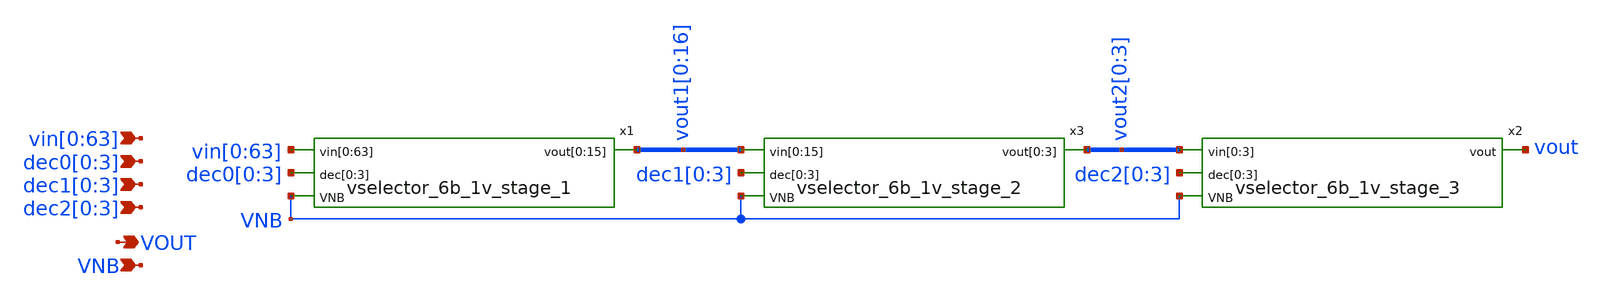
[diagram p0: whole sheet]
** sch_path: xschem/vselector_6b_1v.sch
**.subckt vselector_6b_1v
*+ vin[0],vin[1],vin[2],vin[3],vin[4],vin[5],vin[6],vin[7],vin[8],vin[9],vin[10],vin[11],vin[12],vin[13],vin[14],vin[15],vin[16],vin[17],vin[18],vin[19],vin[20],vin[21],vin[22],vin[23],vin[24],vin[25],vin[26],vin[27],vin[28],vin[29],vin[30],vin[31],vin[32],vin[33],vin[34],vin[35],vin[36],vin[37],vin[38],vin[39],vin[40],vin[41],vin[42],vin[43],vin[44],vin[45],vin[46],vin[47],vin[48],vin[49],vin[50],vin[51],vin[52],vin[53],vin[54],vin[55],vin[56],vin[57],vin[58],vin[59],vin[60],vin[61],vin[62],vin[63] VOUT VNB dec0[0],dec0[1],dec0[2],dec0[3] dec1[0],dec1[1],dec1[2],dec1[3]
*+ dec2[0],dec2[1],dec2[2],dec2[3]
*.ipin
*+ vin[0],vin[1],vin[2],vin[3],vin[4],vin[5],vin[6],vin[7],vin[8],vin[9],vin[10],vin[11],vin[12],vin[13],vin[14],vin[15],vin[16],vin[17],vin[18],vin[19],vin[20],vin[21],vin[22],vin[23],vin[24],vin[25],vin[26],vin[27],vin[28],vin[29],vin[30],vin[31],vin[32],vin[33],vin[34],vin[35],vin[36],vin[37],vin[38],vin[39],vin[40],vin[41],vin[42],vin[43],vin[44],vin[45],vin[46],vin[47],vin[48],vin[49],vin[50],vin[51],vin[52],vin[53],vin[54],vin[55],vin[56],vin[57],vin[58],vin[59],vin[60],vin[61],vin[62],vin[63]
*.opin VOUT
*.ipin VNB
*.ipin dec0[0],dec0[1],dec0[2],dec0[3]
*.ipin dec1[0],dec1[1],dec1[2],dec1[3]
*.ipin dec2[0],dec2[1],dec2[2],dec2[3]
x2 vout2[0] vout2[1] vout2[2] vout2[3] dec2[0] dec2[1] dec2[2] dec2[3] vout VNB
+ vselector_6b_1v_stage_3
x1 vin[0] vin[1] vin[2] vin[3] vin[4] vin[5] vin[6] vin[7] vin[8] vin[9] vin[10] vin[11] vin[12]
+ vin[13] vin[14] vin[15] vin[16] vin[17] vin[18] vin[19] vin[20] vin[21] vin[22] vin[23] vin[24] vin[25]
+ vin[26] vin[27] vin[28] vin[29] vin[30] vin[31] vin[32] vin[33] vin[34] vin[35] vin[36] vin[37] vin[38]
+ vin[39] vin[40] vin[41] vin[42] vin[43] vin[44] vin[45] vin[46] vin[47] vin[48] vin[49] vin[50] vin[51]
+ vin[52] vin[53] vin[54] vin[55] vin[56] vin[57] vin[58] vin[59] vin[60] vin[61] vin[62] vin[63] dec0[0]
+ dec0[1] dec0[2] dec0[3] vout1[0] vout1[1] vout1[2] vout1[3] vout1[4] vout1[5] vout1[6] vout1[7] vout1[8]
+ vout1[9] vout1[10] vout1[11] vout1[12] vout1[13] vout1[14] vout1[15] VNB vselector_6b_1v_stage_1
x3 vout1[0] vout1[1] vout1[2] vout1[3] vout1[4] vout1[5] vout1[6] vout1[7] vout1[8] vout1[9]
+ vout1[10] vout1[11] vout1[12] vout1[13] vout1[14] vout1[15] dec1[0] dec1[1] dec1[2] dec1[3] vout2[0] vout2[1]
+ vout2[2] vout2[3] VNB vselector_6b_1v_stage_2
**.ends

* expanding   symbol:  vselector_6b_1v_stage_3.sym # of pins=4
** sym_path: xschem/vselector_6b_1v_stage_3.sym
** sch_path: xschem/vselector_6b_1v_stage_3.sch
.subckt vselector_6b_1v_stage_3 vin[0] vin[1] vin[2] vin[3] dec[0] dec[1] dec[2] dec[3] vout VNB
*.ipin vin[0],vin[1],vin[2],vin[3]
*.opin vout
*.ipin VNB
*.ipin dec[0],dec[1],dec[2],dec[3]
.param wp=0.42 wn=0.42 l=0.5

XM1 vout dec[0] vin[0] VNB sky130_fd_pr__nfet_g5v0d10v5 L=l W=wn nf=1 ad='int((nf+1)/2) * W/nf * 0.29'
+ as='int((nf+2)/2) * W/nf * 0.29' pd='2*int((nf+1)/2) * (W/nf + 0.29)' ps='2*int((nf+2)/2) * (W/nf + 0.29)'
+ nrd='0.29 / W' nrs='0.29 / W' sa=0 sb=0 sd=0 mult=1 m=1
XM2 vout dec[1] vin[1] VNB sky130_fd_pr__nfet_g5v0d10v5 L=l W=wn nf=1 ad='int((nf+1)/2) * W/nf * 0.29'
+ as='int((nf+2)/2) * W/nf * 0.29' pd='2*int((nf+1)/2) * (W/nf + 0.29)' ps='2*int((nf+2)/2) * (W/nf + 0.29)'
+ nrd='0.29 / W' nrs='0.29 / W' sa=0 sb=0 sd=0 mult=1 m=1
XM3 vout dec[2] vin[2] VNB sky130_fd_pr__nfet_g5v0d10v5 L=l W=wn nf=1 ad='int((nf+1)/2) * W/nf * 0.29'
+ as='int((nf+2)/2) * W/nf * 0.29' pd='2*int((nf+1)/2) * (W/nf + 0.29)' ps='2*int((nf+2)/2) * (W/nf + 0.29)'
+ nrd='0.29 / W' nrs='0.29 / W' sa=0 sb=0 sd=0 mult=1 m=1
XM4 vout dec[3] vin[3] VNB sky130_fd_pr__nfet_g5v0d10v5 L=l W=wn nf=1 ad='int((nf+1)/2) * W/nf * 0.29'
+ as='int((nf+2)/2) * W/nf * 0.29' pd='2*int((nf+1)/2) * (W/nf + 0.29)' ps='2*int((nf+2)/2) * (W/nf + 0.29)'
+ nrd='0.29 / W' nrs='0.29 / W' sa=0 sb=0 sd=0 mult=1 m=1
.ends


* expanding   symbol:  vselector_6b_1v_stage_1.sym # of pins=4
** sym_path: xschem/vselector_6b_1v_stage_1.sym
** sch_path: xschem/vselector_6b_1v_stage_1.sch
.subckt vselector_6b_1v_stage_1 vin[0] vin[1] vin[2] vin[3] vin[4] vin[5] vin[6] vin[7] vin[8]
+ vin[9] vin[10] vin[11] vin[12] vin[13] vin[14] vin[15] vin[16] vin[17] vin[18] vin[19] vin[20] vin[21]
+ vin[22] vin[23] vin[24] vin[25] vin[26] vin[27] vin[28] vin[29] vin[30] vin[31] vin[32] vin[33] vin[34]
+ vin[35] vin[36] vin[37] vin[38] vin[39] vin[40] vin[41] vin[42] vin[43] vin[44] vin[45] vin[46] vin[47]
+ vin[48] vin[49] vin[50] vin[51] vin[52] vin[53] vin[54] vin[55] vin[56] vin[57] vin[58] vin[59] vin[60]
+ vin[61] vin[62] vin[63] dec[0] dec[1] dec[2] dec[3] vout[0] vout[1] vout[2] vout[3] vout[4] vout[5] vout[6]
+ vout[7] vout[8] vout[9] vout[10] vout[11] vout[12] vout[13] vout[14] vout[15] VNB
*.ipin
*+ vin[0],vin[1],vin[2],vin[3],vin[4],vin[5],vin[6],vin[7],vin[8],vin[9],vin[10],vin[11],vin[12],vin[13],vin[14],vin[15],vin[16],vin[17],vin[18],vin[19],vin[20],vin[21],vin[22],vin[23],vin[24],vin[25],vin[26],vin[27],vin[28],vin[29],vin[30],vin[31],vin[32],vin[33],vin[34],vin[35],vin[36],vin[37],vin[38],vin[39],vin[40],vin[41],vin[42],vin[43],vin[44],vin[45],vin[46],vin[47],vin[48],vin[49],vin[50],vin[51],vin[52],vin[53],vin[54],vin[55],vin[56],vin[57],vin[58],vin[59],vin[60],vin[61],vin[62],vin[63]
*.opin
*+ vout[0],vout[1],vout[2],vout[3],vout[4],vout[5],vout[6],vout[7],vout[8],vout[9],vout[10],vout[11],vout[12],vout[13],vout[14],vout[15]
*.ipin VNB
*.ipin dec[0],dec[1],dec[2],dec[3]
x1 vin[48] vin[49] vin[50] vin[51] vin[52] vin[53] vin[54] vin[55] vin[56] vin[57] vin[58] vin[59]
+ vin[60] vin[61] vin[62] vin[63] dec[3] vout[0] vout[1] vout[2] vout[3] vout[4] vout[5] vout[6] vout[7]
+ vout[8] vout[9] vout[10] vout[11] vout[12] vout[13] vout[14] vout[15] VNB vselector_16b_1v
x2 vin[32] vin[33] vin[34] vin[35] vin[36] vin[37] vin[38] vin[39] vin[40] vin[41] vin[42] vin[43]
+ vin[44] vin[45] vin[46] vin[47] dec[2] vout[0] vout[1] vout[2] vout[3] vout[4] vout[5] vout[6] vout[7]
+ vout[8] vout[9] vout[10] vout[11] vout[12] vout[13] vout[14] vout[15] VNB vselector_16b_1v
x3 vin[16] vin[17] vin[18] vin[19] vin[20] vin[21] vin[22] vin[23] vin[24] vin[25] vin[26] vin[27]
+ vin[28] vin[29] vin[30] vin[31] dec[1] vout[0] vout[1] vout[2] vout[3] vout[4] vout[5] vout[6] vout[7]
+ vout[8] vout[9] vout[10] vout[11] vout[12] vout[13] vout[14] vout[15] VNB vselector_16b_1v
x4 vin[0] vin[1] vin[2] vin[3] vin[4] vin[5] vin[6] vin[7] vin[8] vin[9] vin[10] vin[11] vin[12]
+ vin[13] vin[14] vin[15] dec[0] vout[0] vout[1] vout[2] vout[3] vout[4] vout[5] vout[6] vout[7] vout[8]
+ vout[9] vout[10] vout[11] vout[12] vout[13] vout[14] vout[15] VNB vselector_16b_1v
.ends


* expanding   symbol:  vselector_6b_1v_stage_2.sym # of pins=4
** sym_path: xschem/vselector_6b_1v_stage_2.sym
** sch_path: xschem/vselector_6b_1v_stage_2.sch
.subckt vselector_6b_1v_stage_2 vin[0] vin[1] vin[2] vin[3] vin[4] vin[5] vin[6] vin[7] vin[8]
+ vin[9] vin[10] vin[11] vin[12] vin[13] vin[14] vin[15] dec[0] dec[1] dec[2] dec[3] vout[0] vout[1] vout[2]
+ vout[3] VNB
*.ipin
*+ vin[0],vin[1],vin[2],vin[3],vin[4],vin[5],vin[6],vin[7],vin[8],vin[9],vin[10],vin[11],vin[12],vin[13],vin[14],vin[15]
*.opin vout[0],vout[1],vout[2],vout[3]
*.ipin VNB
*.ipin dec[0],dec[1],dec[2],dec[3]
x1 vin[0] vin[1] vin[2] vin[3] dec[0] vout[0] vout[1] vout[2] vout[3] VNB vselector_4b_1v
x2 vin[4] vin[5] vin[6] vin[7] dec[1] vout[0] vout[1] vout[2] vout[3] VNB vselector_4b_1v
x3 vin[8] vin[9] vin[10] vin[11] dec[2] vout[0] vout[1] vout[2] vout[3] VNB vselector_4b_1v
x4 vin[12] vin[13] vin[14] vin[15] dec[3] vout[0] vout[1] vout[2] vout[3] VNB vselector_4b_1v
.ends


* expanding   symbol:  vselector_16b_1v.sym # of pins=4
** sym_path: xschem/vselector_16b_1v.sym
** sch_path: xschem/vselector_16b_1v.sch
.subckt vselector_16b_1v vin[0] vin[1] vin[2] vin[3] vin[4] vin[5] vin[6] vin[7] vin[8] vin[9]
+ vin[10] vin[11] vin[12] vin[13] vin[14] vin[15] DIN vout[0] vout[1] vout[2] vout[3] vout[4] vout[5] vout[6]
+ vout[7] vout[8] vout[9] vout[10] vout[11] vout[12] vout[13] vout[14] vout[15] VNB
*.ipin
*+ vin[0],vin[1],vin[2],vin[3],vin[4],vin[5],vin[6],vin[7],vin[8],vin[9],vin[10],vin[11],vin[12],vin[13],vin[14],vin[15]
*.opin
*+ vout[0],vout[1],vout[2],vout[3],vout[4],vout[5],vout[6],vout[7],vout[8],vout[9],vout[10],vout[11],vout[12],vout[13],vout[14],vout[15]
*.ipin VNB
*.ipin DIN
.param wp=0.42 wn=0.42 l=0.5

XM1 vout[0] DIN vin[0] VNB sky130_fd_pr__nfet_g5v0d10v5 L=l W=wn nf=1 ad='int((nf+1)/2) * W/nf * 0.29'
+ as='int((nf+2)/2) * W/nf * 0.29' pd='2*int((nf+1)/2) * (W/nf + 0.29)' ps='2*int((nf+2)/2) * (W/nf + 0.29)'
+ nrd='0.29 / W' nrs='0.29 / W' sa=0 sb=0 sd=0 mult=1 m=1
XM2 vout[1] DIN vin[1] VNB sky130_fd_pr__nfet_g5v0d10v5 L=l W=wn nf=1 ad='int((nf+1)/2) * W/nf * 0.29'
+ as='int((nf+2)/2) * W/nf * 0.29' pd='2*int((nf+1)/2) * (W/nf + 0.29)' ps='2*int((nf+2)/2) * (W/nf + 0.29)'
+ nrd='0.29 / W' nrs='0.29 / W' sa=0 sb=0 sd=0 mult=1 m=1
XM3 vout[2] DIN vin[2] VNB sky130_fd_pr__nfet_g5v0d10v5 L=l W=wn nf=1 ad='int((nf+1)/2) * W/nf * 0.29'
+ as='int((nf+2)/2) * W/nf * 0.29' pd='2*int((nf+1)/2) * (W/nf + 0.29)' ps='2*int((nf+2)/2) * (W/nf + 0.29)'
+ nrd='0.29 / W' nrs='0.29 / W' sa=0 sb=0 sd=0 mult=1 m=1
XM4 vout[3] DIN vin[3] VNB sky130_fd_pr__nfet_g5v0d10v5 L=l W=wn nf=1 ad='int((nf+1)/2) * W/nf * 0.29'
+ as='int((nf+2)/2) * W/nf * 0.29' pd='2*int((nf+1)/2) * (W/nf + 0.29)' ps='2*int((nf+2)/2) * (W/nf + 0.29)'
+ nrd='0.29 / W' nrs='0.29 / W' sa=0 sb=0 sd=0 mult=1 m=1
XM5 vout[4] DIN vin[4] VNB sky130_fd_pr__nfet_g5v0d10v5 L=l W=wn nf=1 ad='int((nf+1)/2) * W/nf * 0.29'
+ as='int((nf+2)/2) * W/nf * 0.29' pd='2*int((nf+1)/2) * (W/nf + 0.29)' ps='2*int((nf+2)/2) * (W/nf + 0.29)'
+ nrd='0.29 / W' nrs='0.29 / W' sa=0 sb=0 sd=0 mult=1 m=1
XM6 vout[5] DIN vin[5] VNB sky130_fd_pr__nfet_g5v0d10v5 L=l W=wn nf=1 ad='int((nf+1)/2) * W/nf * 0.29'
+ as='int((nf+2)/2) * W/nf * 0.29' pd='2*int((nf+1)/2) * (W/nf + 0.29)' ps='2*int((nf+2)/2) * (W/nf + 0.29)'
+ nrd='0.29 / W' nrs='0.29 / W' sa=0 sb=0 sd=0 mult=1 m=1
XM7 vout[6] DIN vin[6] VNB sky130_fd_pr__nfet_g5v0d10v5 L=l W=wn nf=1 ad='int((nf+1)/2) * W/nf * 0.29'
+ as='int((nf+2)/2) * W/nf * 0.29' pd='2*int((nf+1)/2) * (W/nf + 0.29)' ps='2*int((nf+2)/2) * (W/nf + 0.29)'
+ nrd='0.29 / W' nrs='0.29 / W' sa=0 sb=0 sd=0 mult=1 m=1
XM8 vout[7] DIN vin[7] VNB sky130_fd_pr__nfet_g5v0d10v5 L=l W=wn nf=1 ad='int((nf+1)/2) * W/nf * 0.29'
+ as='int((nf+2)/2) * W/nf * 0.29' pd='2*int((nf+1)/2) * (W/nf + 0.29)' ps='2*int((nf+2)/2) * (W/nf + 0.29)'
+ nrd='0.29 / W' nrs='0.29 / W' sa=0 sb=0 sd=0 mult=1 m=1
XM9 vout[8] DIN vin[8] VNB sky130_fd_pr__nfet_g5v0d10v5 L=l W=wn nf=1 ad='int((nf+1)/2) * W/nf * 0.29'
+ as='int((nf+2)/2) * W/nf * 0.29' pd='2*int((nf+1)/2) * (W/nf + 0.29)' ps='2*int((nf+2)/2) * (W/nf + 0.29)'
+ nrd='0.29 / W' nrs='0.29 / W' sa=0 sb=0 sd=0 mult=1 m=1
XM10 vout[9] DIN vin[9] VNB sky130_fd_pr__nfet_g5v0d10v5 L=l W=wn nf=1 ad='int((nf+1)/2) * W/nf * 0.29'
+ as='int((nf+2)/2) * W/nf * 0.29' pd='2*int((nf+1)/2) * (W/nf + 0.29)' ps='2*int((nf+2)/2) * (W/nf + 0.29)'
+ nrd='0.29 / W' nrs='0.29 / W' sa=0 sb=0 sd=0 mult=1 m=1
XM11 vout[10] DIN vin[10] VNB sky130_fd_pr__nfet_g5v0d10v5 L=l W=wn nf=1 ad='int((nf+1)/2) * W/nf * 0.29'
+ as='int((nf+2)/2) * W/nf * 0.29' pd='2*int((nf+1)/2) * (W/nf + 0.29)' ps='2*int((nf+2)/2) * (W/nf + 0.29)'
+ nrd='0.29 / W' nrs='0.29 / W' sa=0 sb=0 sd=0 mult=1 m=1
XM12 vout[11] DIN vin[11] VNB sky130_fd_pr__nfet_g5v0d10v5 L=l W=wn nf=1 ad='int((nf+1)/2) * W/nf * 0.29'
+ as='int((nf+2)/2) * W/nf * 0.29' pd='2*int((nf+1)/2) * (W/nf + 0.29)' ps='2*int((nf+2)/2) * (W/nf + 0.29)'
+ nrd='0.29 / W' nrs='0.29 / W' sa=0 sb=0 sd=0 mult=1 m=1
XM13 vout[12] DIN vin[12] VNB sky130_fd_pr__nfet_g5v0d10v5 L=l W=wn nf=1 ad='int((nf+1)/2) * W/nf * 0.29'
+ as='int((nf+2)/2) * W/nf * 0.29' pd='2*int((nf+1)/2) * (W/nf + 0.29)' ps='2*int((nf+2)/2) * (W/nf + 0.29)'
+ nrd='0.29 / W' nrs='0.29 / W' sa=0 sb=0 sd=0 mult=1 m=1
XM14 vout[13] DIN vin[13] VNB sky130_fd_pr__nfet_g5v0d10v5 L=l W=wn nf=1 ad='int((nf+1)/2) * W/nf * 0.29'
+ as='int((nf+2)/2) * W/nf * 0.29' pd='2*int((nf+1)/2) * (W/nf + 0.29)' ps='2*int((nf+2)/2) * (W/nf + 0.29)'
+ nrd='0.29 / W' nrs='0.29 / W' sa=0 sb=0 sd=0 mult=1 m=1
XM15 vout[14] DIN vin[14] VNB sky130_fd_pr__nfet_g5v0d10v5 L=l W=wn nf=1 ad='int((nf+1)/2) * W/nf * 0.29'
+ as='int((nf+2)/2) * W/nf * 0.29' pd='2*int((nf+1)/2) * (W/nf + 0.29)' ps='2*int((nf+2)/2) * (W/nf + 0.29)'
+ nrd='0.29 / W' nrs='0.29 / W' sa=0 sb=0 sd=0 mult=1 m=1
XM16 vout[15] DIN vin[15] VNB sky130_fd_pr__nfet_g5v0d10v5 L=l W=wn nf=1 ad='int((nf+1)/2) * W/nf * 0.29'
+ as='int((nf+2)/2) * W/nf * 0.29' pd='2*int((nf+1)/2) * (W/nf + 0.29)' ps='2*int((nf+2)/2) * (W/nf + 0.29)'
+ nrd='0.29 / W' nrs='0.29 / W' sa=0 sb=0 sd=0 mult=1 m=1
.ends


* expanding   symbol:  vselector_4b_1v.sym # of pins=4
** sym_path: xschem/vselector_4b_1v.sym
** sch_path: xschem/vselector_4b_1v.sch
.subckt vselector_4b_1v vin[0] vin[1] vin[2] vin[3] DIN vout[0] vout[1] vout[2] vout[3] VNB
*.ipin vin[0],vin[1],vin[2],vin[3]
*.opin vout[0],vout[1],vout[2],vout[3]
*.ipin VNB
*.ipin DIN
.param wp=0.42 wn=0.42 l=0.5

XM1 vout[0] DIN vin[0] VNB sky130_fd_pr__nfet_g5v0d10v5 L=l W=wn nf=1 ad='int((nf+1)/2) * W/nf * 0.29'
+ as='int((nf+2)/2) * W/nf * 0.29' pd='2*int((nf+1)/2) * (W/nf + 0.29)' ps='2*int((nf+2)/2) * (W/nf + 0.29)'
+ nrd='0.29 / W' nrs='0.29 / W' sa=0 sb=0 sd=0 mult=1 m=1
XM2 vout[1] DIN vin[1] VNB sky130_fd_pr__nfet_g5v0d10v5 L=l W=wn nf=1 ad='int((nf+1)/2) * W/nf * 0.29'
+ as='int((nf+2)/2) * W/nf * 0.29' pd='2*int((nf+1)/2) * (W/nf + 0.29)' ps='2*int((nf+2)/2) * (W/nf + 0.29)'
+ nrd='0.29 / W' nrs='0.29 / W' sa=0 sb=0 sd=0 mult=1 m=1
XM3 vout[2] DIN vin[2] VNB sky130_fd_pr__nfet_g5v0d10v5 L=l W=wn nf=1 ad='int((nf+1)/2) * W/nf * 0.29'
+ as='int((nf+2)/2) * W/nf * 0.29' pd='2*int((nf+1)/2) * (W/nf + 0.29)' ps='2*int((nf+2)/2) * (W/nf + 0.29)'
+ nrd='0.29 / W' nrs='0.29 / W' sa=0 sb=0 sd=0 mult=1 m=1
XM4 vout[3] DIN vin[3] VNB sky130_fd_pr__nfet_g5v0d10v5 L=l W=wn nf=1 ad='int((nf+1)/2) * W/nf * 0.29'
+ as='int((nf+2)/2) * W/nf * 0.29' pd='2*int((nf+1)/2) * (W/nf + 0.29)' ps='2*int((nf+2)/2) * (W/nf + 0.29)'
+ nrd='0.29 / W' nrs='0.29 / W' sa=0 sb=0 sd=0 mult=1 m=1
.ends

.end
